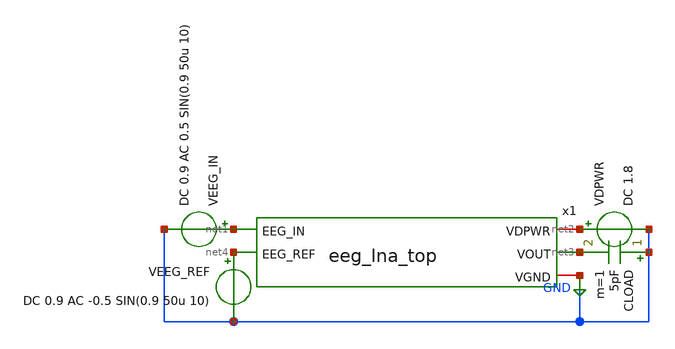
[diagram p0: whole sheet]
** sch_path: xschem/tb_eeg_lna_top.sch
**.subckt tb_eeg_lna_top
x1 net1 net2 net3 GND net4 eeg_lna_top
VDPWR net2 GND DC 1.8
VEEG_REF net4 GND DC 0.9 AC -0.5 SIN(0.9 50u 10)
VEEG_IN net1 GND DC 0.9 AC 0.5 SIN(0.9 50u 10)
CLOAD GND net3 5pF m=1
**** begin user architecture code


.lib /foss/pdks/sky130A/libs.tech/ngspice/sky130.lib.spice tt

.option savecurrents

* tiny DC leak paths for convergence only
RLEAKP x1.ota_inp GND 1T
RLEAKN x1.ota_inn GND 1T

.control

op

print v(x1.vcm)
print v(x1.ota_inp)
print v(x1.ota_inn)
print v(net3)

* allow huge RC startup to settle
tran 10m 20

* actual differential input signal
plot v(net1)-v(net4)

* OTA input common-mode behavior
plot v(x1.ota_inp)
plot v(x1.ota_inn)

* output waveform
plot v(net3)

* centered around VCM
plot v(net3)-0.9

* proper closed-loop gain measurement
ac dec 100 0.01 100k

plot db(v(net3)/(v(net1)-v(net4)))

.endc


**** end user architecture code
**.ends

* expanding   symbol:  eeg_lna_top.sym # of pins=5
** sym_path: xschem/eeg_lna_top.sym
** sch_path: xschem/eeg_lna_top.sch
.subckt eeg_lna_top EEG_IN VDPWR VOUT VGND EEG_REF
*.ipin EEG_IN
*.ipin EEG_REF
*.iopin VDPWR
*.iopin VGND
*.opin VOUT
x2 net3 net4 pseudo_res
x1 net5 net6 pseudo_res
XCACP EEG_IN net2 sky130_fd_pr__cap_mim_m3_1 W=1 L=1 MF=1 m=1
XC_REF EEG_REF net1 sky130_fd_pr__cap_mim_m3_1 W=1 L=1 MF=1 m=1
x3 net7 net8 net2 net1 net9 net10 ota_5t
.ends


* expanding   symbol:  pseudo_res.sym # of pins=2
** sym_path: xschem/pseudo_res.sym
** sch_path: xschem/pseudo_res.sch
.subckt pseudo_res B A
*.iopin A
*.iopin B
XM1_PSEUDO_RES B B A A sky130_fd_pr__pfet_01v8 L=10 W=0.42 nf=1 ad='int((1 + 1)/2) * 0.42 / 1 * 0.29'
+ as='int((1 + 2)/2) * 0.42 / 1 * 0.29' pd='2*int((1 + 1)/2) * (0.42 / 1 + 0.29)' ps='2*int((1 + 2)/2) * (0.42 / 1 + 0.29)'
+ nrd='0.29 / 0.42 ' nrs='0.29 / 0.42 ' sa=0 sb=0 sd=0 mult=1 m=1
XM2_PSEUDO_RES A A B B sky130_fd_pr__pfet_01v8 L=10 W=0.42 nf=1 ad='int((1 + 1)/2) * 0.42 / 1 * 0.29'
+ as='int((1 + 2)/2) * 0.42 / 1 * 0.29' pd='2*int((1 + 1)/2) * (0.42 / 1 + 0.29)' ps='2*int((1 + 2)/2) * (0.42 / 1 + 0.29)'
+ nrd='0.29 / 0.42 ' nrs='0.29 / 0.42 ' sa=0 sb=0 sd=0 mult=1 m=1
.ends


* expanding   symbol:  ota_5t.sym # of pins=6
** sym_path: xschem-new/ota_5t.sym
** sch_path: xschem-new/ota_5t.sch
.subckt ota_5t BIAS_P VDPWR VIN_P VIN_N VOUT VGND
*.ipin VIN_P
*.ipin VIN_N
*.ipin BIAS_P
*.iopin VDPWR
*.iopin VGND
*.opin VOUT
XMDIFF_P net1 VIN_P TAIL_P VDPWR sky130_fd_pr__pfet_01v8 L=4 W=48 nf=1 ad='int((1 + 1)/2) * 48 / 1 * 0.29'
+ as='int((1 + 2)/2) * 48 / 1 * 0.29' pd='2*int((1 + 1)/2) * (48 / 1 + 0.29)' ps='2*int((1 + 2)/2) * (48 / 1 + 0.29)'
+ nrd='0.29 / 48 ' nrs='0.29 / 48 ' sa=0 sb=0 sd=0 mult=1 m=1
XMDIFF_N VOUT VIN_N TAIL_P VDPWR sky130_fd_pr__pfet_01v8 L=4 W=48 nf=1 ad='int((1 + 1)/2) * 48 / 1 * 0.29'
+ as='int((1 + 2)/2) * 48 / 1 * 0.29' pd='2*int((1 + 1)/2) * (48 / 1 + 0.29)' ps='2*int((1 + 2)/2) * (48 / 1 + 0.29)'
+ nrd='0.29 / 48 ' nrs='0.29 / 48 ' sa=0 sb=0 sd=0 mult=1 m=1
XMTAIL TAIL_P BIAS_P VDPWR VDPWR sky130_fd_pr__pfet_01v8 L=8 W=0.5 nf=1 ad='int((1 + 1)/2) * 0.5 / 1 * 0.29'
+ as='int((1 + 2)/2) * 0.5 / 1 * 0.29' pd='2*int((1 + 1)/2) * (0.5 / 1 + 0.29)' ps='2*int((1 + 2)/2) * (0.5 / 1 + 0.29)'
+ nrd='0.29 / 0.5 ' nrs='0.29 / 0.5 ' sa=0 sb=0 sd=0 mult=1 m=1
XMLOAD_REF net1 net1 VGND VGND sky130_fd_pr__nfet_01v8 L=16 W=8 nf=1 ad='int((1 + 1)/2) * 8 / 1 * 0.29'
+ as='int((1 + 2)/2) * 8 / 1 * 0.29' pd='2*int((1 + 1)/2) * (8 / 1 + 0.29)' ps='2*int((1 + 2)/2) * (8 / 1 + 0.29)'
+ nrd='0.29 / 8 ' nrs='0.29 / 8 ' sa=0 sb=0 sd=0 mult=1 m=1
XMLOAD_OUT VOUT net1 VGND VGND sky130_fd_pr__nfet_01v8 L=16 W=8 nf=1 ad='int((1 + 1)/2) * 8 / 1 * 0.29'
+ as='int((1 + 2)/2) * 8 / 1 * 0.29' pd='2*int((1 + 1)/2) * (8 / 1 + 0.29)' ps='2*int((1 + 2)/2) * (8 / 1 + 0.29)'
+ nrd='0.29 / 8 ' nrs='0.29 / 8 ' sa=0 sb=0 sd=0 mult=1 m=1
.ends

.GLOBAL GND
.end
